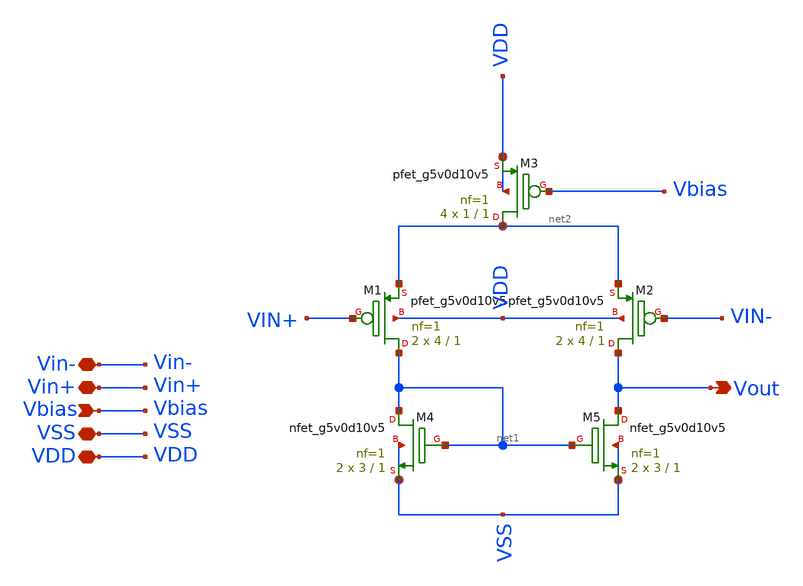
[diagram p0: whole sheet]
** sch_path: xschem/Amplifiers/5Tpi.sch
**.subckt 5Tpi Vin- Vin+ Vbias VSS VDD Vout
*.iopin Vin-
*.iopin Vin+
*.ipin Vbias
*.iopin VSS
*.iopin VDD
*.opin Vout
XM1 net1 VIN+ net2 VDD sky130_fd_pr__pfet_g5v0d10v5 L=1 W=4 nf=1 ad='int((nf+1)/2) * W/nf * 0.29' as='int((nf+2)/2) * W/nf * 0.29'
+ pd='2*int((nf+1)/2) * (W/nf + 0.29)' ps='2*int((nf+2)/2) * (W/nf + 0.29)' nrd='0.29 / W' nrs='0.29 / W'
+ sa=0 sb=0 sd=0 mult=2 m=2
XM2 Vout VIN- net2 VDD sky130_fd_pr__pfet_g5v0d10v5 L=1 W=4 nf=1 ad='int((nf+1)/2) * W/nf * 0.29' as='int((nf+2)/2) * W/nf * 0.29'
+ pd='2*int((nf+1)/2) * (W/nf + 0.29)' ps='2*int((nf+2)/2) * (W/nf + 0.29)' nrd='0.29 / W' nrs='0.29 / W'
+ sa=0 sb=0 sd=0 mult=2 m=2
XM3 net2 Vbias VDD VDD sky130_fd_pr__pfet_g5v0d10v5 L=1 W=1 nf=1 ad='int((nf+1)/2) * W/nf * 0.29' as='int((nf+2)/2) * W/nf * 0.29'
+ pd='2*int((nf+1)/2) * (W/nf + 0.29)' ps='2*int((nf+2)/2) * (W/nf + 0.29)' nrd='0.29 / W' nrs='0.29 / W'
+ sa=0 sb=0 sd=0 mult=4 m=4
XM4 net1 net1 VSS VSS sky130_fd_pr__nfet_g5v0d10v5 L=1 W=3 nf=1 ad='int((nf+1)/2) * W/nf * 0.29' as='int((nf+2)/2) * W/nf * 0.29'
+ pd='2*int((nf+1)/2) * (W/nf + 0.29)' ps='2*int((nf+2)/2) * (W/nf + 0.29)' nrd='0.29 / W' nrs='0.29 / W'
+ sa=0 sb=0 sd=0 mult=2 m=2
XM5 Vout net1 VSS VSS sky130_fd_pr__nfet_g5v0d10v5 L=1 W=3 nf=1 ad='int((nf+1)/2) * W/nf * 0.29' as='int((nf+2)/2) * W/nf * 0.29'
+ pd='2*int((nf+1)/2) * (W/nf + 0.29)' ps='2*int((nf+2)/2) * (W/nf + 0.29)' nrd='0.29 / W' nrs='0.29 / W'
+ sa=0 sb=0 sd=0 mult=2 m=2
**.ends
.end
